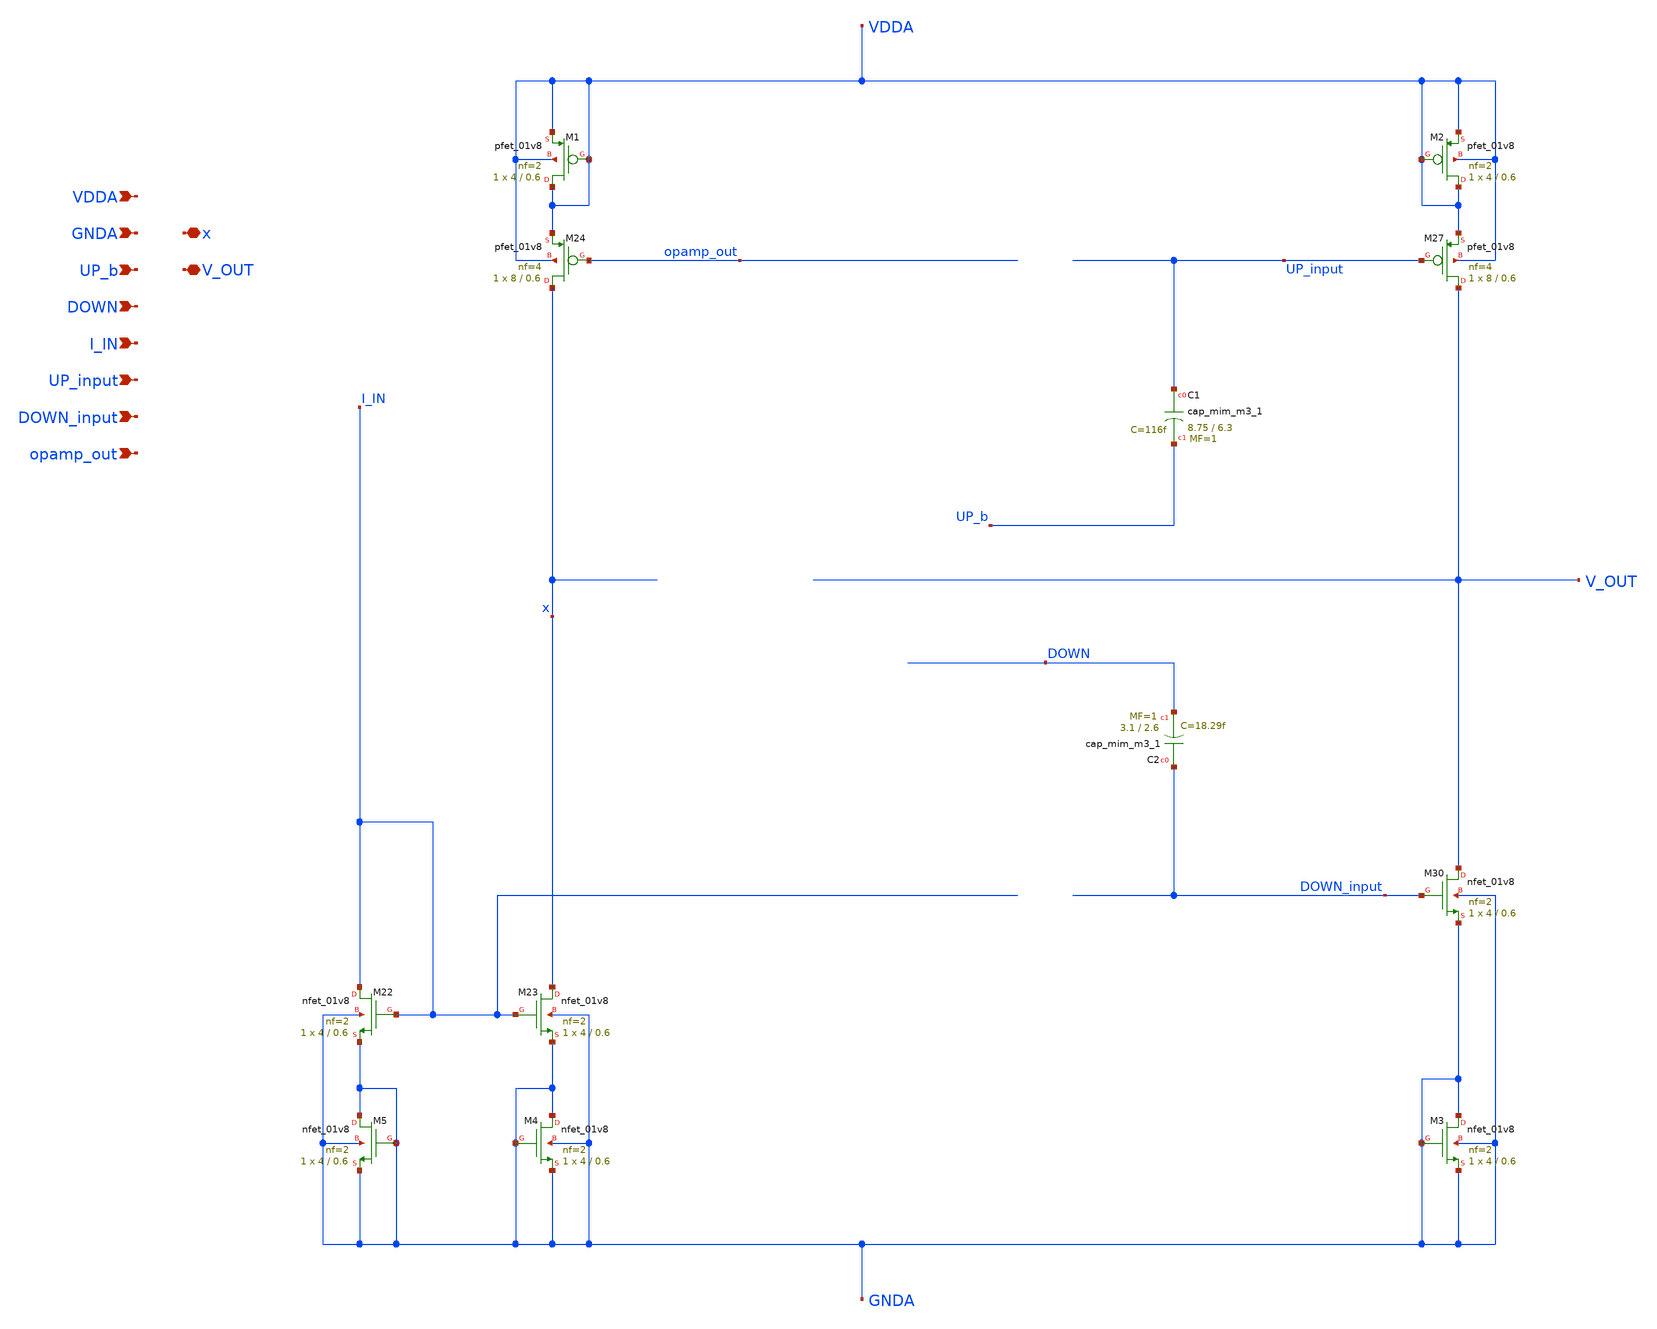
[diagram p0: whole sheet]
** sch_path: projects/pll/charge_pump/magic/charge_pump_xschem_3.sch
**.subckt charge_pump_xschem_3 VDDA GNDA UP_b DOWN I_IN x V_OUT UP_input DOWN_input opamp_out
*.ipin VDDA
*.ipin GNDA
*.ipin UP_b
*.ipin DOWN
*.ipin I_IN
*.iopin x
*.iopin V_OUT
*.ipin UP_input
*.ipin DOWN_input
*.ipin opamp_out
XM22 I_IN I_IN GNDA GNDA sky130_fd_pr__nfet_01v8 L=0.6 W=4 nf=2 ad='int((nf+1)/2) * W/nf * 0.29' as='int((nf+2)/2) * W/nf * 0.29'
+ pd='2*int((nf+1)/2) * (W/nf + 0.29)' ps='2*int((nf+2)/2) * (W/nf + 0.29)' nrd='0.29 / W' nrs='0.29 / W'
+ sa=0 sb=0 sd=0 mult=1 m=1
XM23 x I_IN GNDA GNDA sky130_fd_pr__nfet_01v8 L=0.6 W=4 nf=2 ad='int((nf+1)/2) * W/nf * 0.29' as='int((nf+2)/2) * W/nf * 0.29'
+ pd='2*int((nf+1)/2) * (W/nf + 0.29)' ps='2*int((nf+2)/2) * (W/nf + 0.29)' nrd='0.29 / W' nrs='0.29 / W'
+ sa=0 sb=0 sd=0 mult=1 m=1
XM24 x opamp_out VDDA VDDA sky130_fd_pr__pfet_01v8 L=0.6 W=8 nf=4 ad='int((nf+1)/2) * W/nf * 0.29' as='int((nf+2)/2) * W/nf * 0.29'
+ pd='2*int((nf+1)/2) * (W/nf + 0.29)' ps='2*int((nf+2)/2) * (W/nf + 0.29)' nrd='0.29 / W' nrs='0.29 / W'
+ sa=0 sb=0 sd=0 mult=1 m=1
XM27 V_OUT UP_input VDDA VDDA sky130_fd_pr__pfet_01v8 L=0.6 W=8 nf=4 ad='int((nf+1)/2) * W/nf * 0.29'
+ as='int((nf+2)/2) * W/nf * 0.29' pd='2*int((nf+1)/2) * (W/nf + 0.29)' ps='2*int((nf+2)/2) * (W/nf + 0.29)'
+ nrd='0.29 / W' nrs='0.29 / W' sa=0 sb=0 sd=0 mult=1 m=1
XM30 V_OUT DOWN_input GNDA GNDA sky130_fd_pr__nfet_01v8 L=0.6 W=4 nf=2 ad='int((nf+1)/2) * W/nf * 0.29'
+ as='int((nf+2)/2) * W/nf * 0.29' pd='2*int((nf+1)/2) * (W/nf + 0.29)' ps='2*int((nf+2)/2) * (W/nf + 0.29)'
+ nrd='0.29 / W' nrs='0.29 / W' sa=0 sb=0 sd=0 mult=1 m=1
XC1 UP_input UP_b sky130_fd_pr__cap_mim_m3_1 W=8.75 L=6.3 MF=1 m=1
XC2 DOWN_input DOWN sky130_fd_pr__cap_mim_m3_1 W=3.1 L=2.6 MF=1 m=1
XM1 VDDA VDDA VDDA VDDA sky130_fd_pr__pfet_01v8 L=0.6 W=4 nf=2 ad='int((nf+1)/2) * W/nf * 0.29' as='int((nf+2)/2) * W/nf * 0.29'
+ pd='2*int((nf+1)/2) * (W/nf + 0.29)' ps='2*int((nf+2)/2) * (W/nf + 0.29)' nrd='0.29 / W' nrs='0.29 / W'
+ sa=0 sb=0 sd=0 mult=1 m=1
XM2 VDDA VDDA VDDA VDDA sky130_fd_pr__pfet_01v8 L=0.6 W=4 nf=2 ad='int((nf+1)/2) * W/nf * 0.29' as='int((nf+2)/2) * W/nf * 0.29'
+ pd='2*int((nf+1)/2) * (W/nf + 0.29)' ps='2*int((nf+2)/2) * (W/nf + 0.29)' nrd='0.29 / W' nrs='0.29 / W'
+ sa=0 sb=0 sd=0 mult=1 m=1
XM3 GNDA GNDA GNDA GNDA sky130_fd_pr__nfet_01v8 L=0.6 W=4 nf=2 ad='int((nf+1)/2) * W/nf * 0.29' as='int((nf+2)/2) * W/nf * 0.29'
+ pd='2*int((nf+1)/2) * (W/nf + 0.29)' ps='2*int((nf+2)/2) * (W/nf + 0.29)' nrd='0.29 / W' nrs='0.29 / W'
+ sa=0 sb=0 sd=0 mult=1 m=1
XM4 GNDA GNDA GNDA GNDA sky130_fd_pr__nfet_01v8 L=0.6 W=4 nf=2 ad='int((nf+1)/2) * W/nf * 0.29' as='int((nf+2)/2) * W/nf * 0.29'
+ pd='2*int((nf+1)/2) * (W/nf + 0.29)' ps='2*int((nf+2)/2) * (W/nf + 0.29)' nrd='0.29 / W' nrs='0.29 / W'
+ sa=0 sb=0 sd=0 mult=1 m=1
XM5 GNDA GNDA GNDA GNDA sky130_fd_pr__nfet_01v8 L=0.6 W=4 nf=2 ad='int((nf+1)/2) * W/nf * 0.29' as='int((nf+2)/2) * W/nf * 0.29'
+ pd='2*int((nf+1)/2) * (W/nf + 0.29)' ps='2*int((nf+2)/2) * (W/nf + 0.29)' nrd='0.29 / W' nrs='0.29 / W'
+ sa=0 sb=0 sd=0 mult=1 m=1
**.ends
.end
